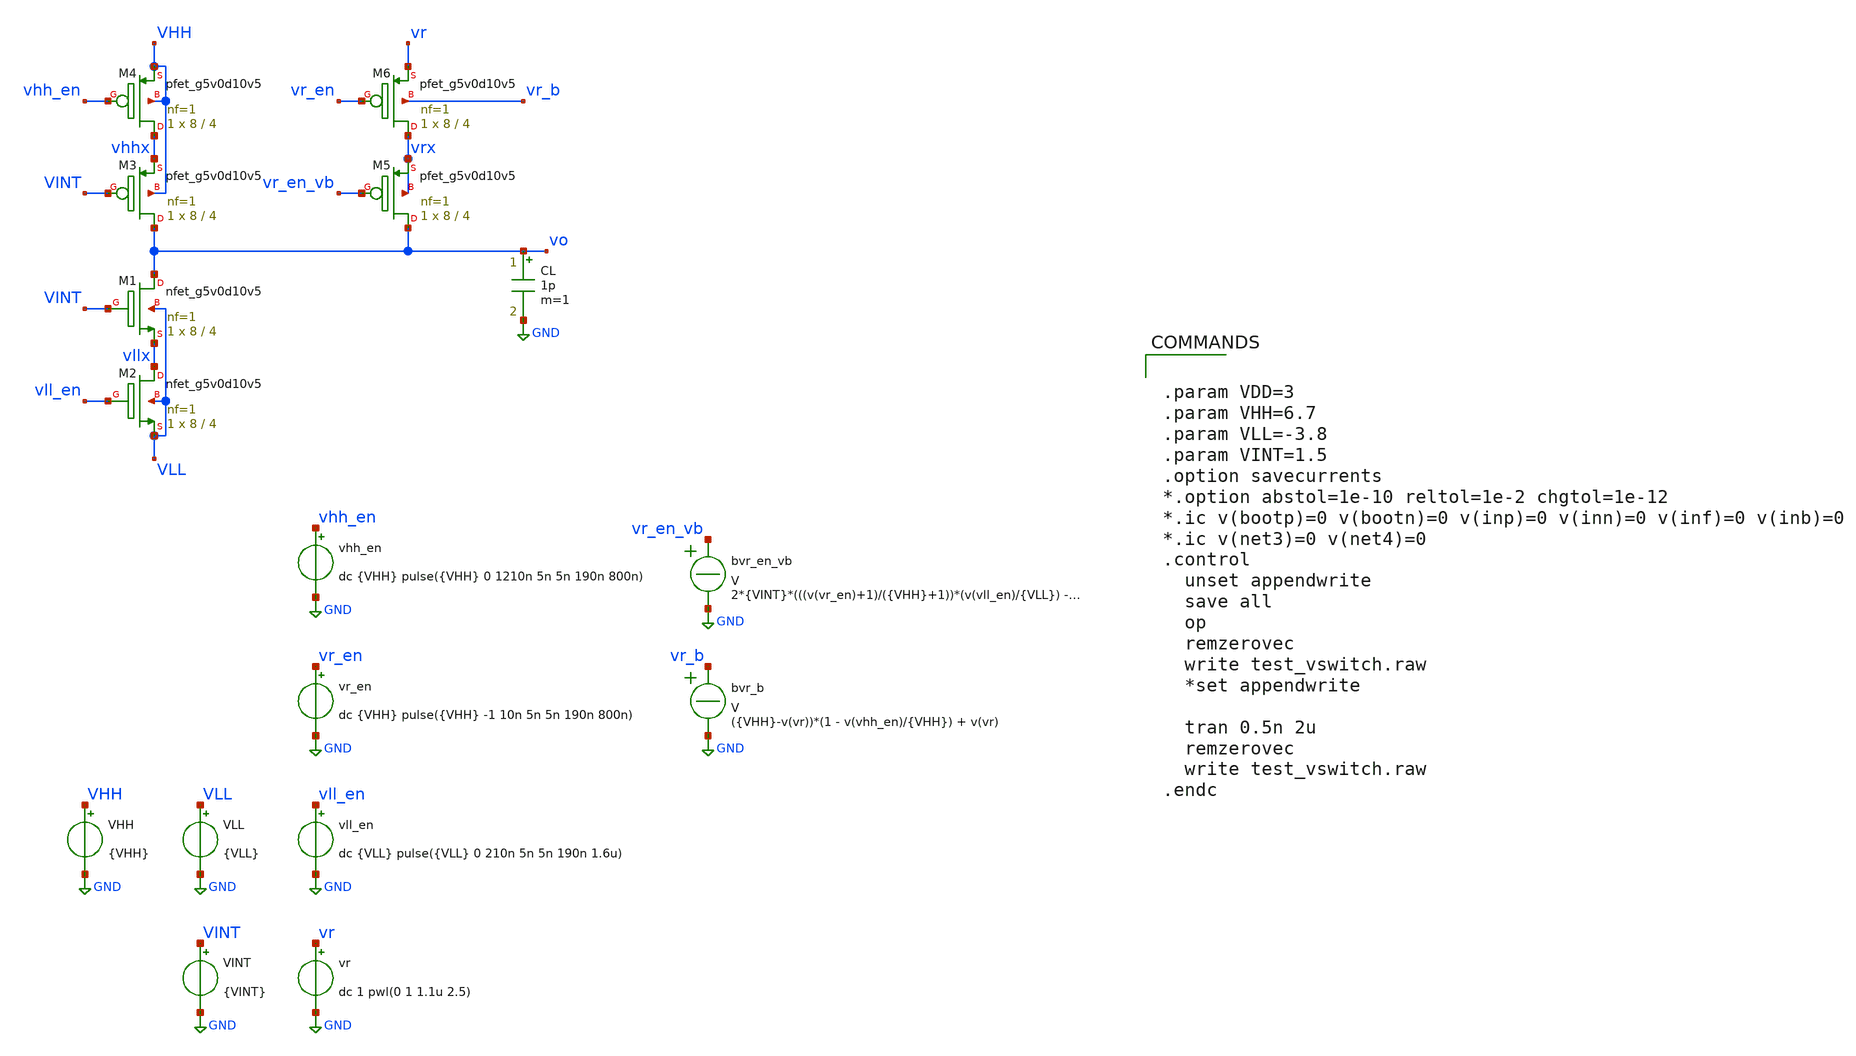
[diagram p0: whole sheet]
** sch_path: analog_switch/test_vswitch.sch
**.subckt test_vswitch
XM1 vo VINT vllx VLL sky130_fd_pr__nfet_g5v0d10v5 L=4 W=8 nf=1 ad='int((nf+1)/2) * W/nf * 0.29' as='int((nf+2)/2) * W/nf * 0.29'
+ pd='2*int((nf+1)/2) * (W/nf + 0.29)' ps='2*int((nf+2)/2) * (W/nf + 0.29)' nrd='0.29 / W' nrs='0.29 / W'
+ sa=0 sb=0 sd=0 mult=1 m=1
XM2 vllx vll_en VLL VLL sky130_fd_pr__nfet_g5v0d10v5 L=4 W=8 nf=1 ad='int((nf+1)/2) * W/nf * 0.29' as='int((nf+2)/2) * W/nf * 0.29'
+ pd='2*int((nf+1)/2) * (W/nf + 0.29)' ps='2*int((nf+2)/2) * (W/nf + 0.29)' nrd='0.29 / W' nrs='0.29 / W'
+ sa=0 sb=0 sd=0 mult=1 m=1
XM3 vo VINT vhhx VHH sky130_fd_pr__pfet_g5v0d10v5 L=4 W=8 nf=1 ad='int((nf+1)/2) * W/nf * 0.29' as='int((nf+2)/2) * W/nf * 0.29'
+ pd='2*int((nf+1)/2) * (W/nf + 0.29)' ps='2*int((nf+2)/2) * (W/nf + 0.29)' nrd='0.29 / W' nrs='0.29 / W'
+ sa=0 sb=0 sd=0 mult=1 m=1
XM4 vhhx vhh_en VHH VHH sky130_fd_pr__pfet_g5v0d10v5 L=4 W=8 nf=1 ad='int((nf+1)/2) * W/nf * 0.29' as='int((nf+2)/2) * W/nf * 0.29'
+ pd='2*int((nf+1)/2) * (W/nf + 0.29)' ps='2*int((nf+2)/2) * (W/nf + 0.29)' nrd='0.29 / W' nrs='0.29 / W'
+ sa=0 sb=0 sd=0 mult=1 m=1
XM5 vo vr_en_vb vrx vrx sky130_fd_pr__pfet_g5v0d10v5 L=4 W=8 nf=1 ad='int((nf+1)/2) * W/nf * 0.29' as='int((nf+2)/2) * W/nf * 0.29'
+ pd='2*int((nf+1)/2) * (W/nf + 0.29)' ps='2*int((nf+2)/2) * (W/nf + 0.29)' nrd='0.29 / W' nrs='0.29 / W'
+ sa=0 sb=0 sd=0 mult=1 m=1
XM6 vrx vr_en vr vr_b sky130_fd_pr__pfet_g5v0d10v5 L=4 W=8 nf=1 ad='int((nf+1)/2) * W/nf * 0.29' as='int((nf+2)/2) * W/nf * 0.29'
+ pd='2*int((nf+1)/2) * (W/nf + 0.29)' ps='2*int((nf+2)/2) * (W/nf + 0.29)' nrd='0.29 / W' nrs='0.29 / W'
+ sa=0 sb=0 sd=0 mult=1 m=1
VHH VHH GND {VHH}
VLL VLL GND {VLL}
vr vr GND dc 1 pwl(0 1 1.1u 2.5)
VINT VINT GND {VINT}
vll_en vll_en GND dc {VLL} pulse({VLL} 0 210n 5n 5n 190n 1.6u)
vr_en vr_en GND dc {VHH} pulse({VHH} -1 10n 5n 5n 190n 800n)
vhh_en vhh_en GND dc {VHH} pulse({VHH} 0 1210n 5n 5n 190n 800n)
bvr_en_vb vr_en_vb GND V = 2*{VINT}*(((v(vr_en)+1)/({VHH}+1))*(v(vll_en)/{VLL}) - 0.5)
CL vo GND 1p m=1
bvr_b vr_b GND V = ({VHH}-v(vr))*(1 - v(vhh_en)/{VHH}) + v(vr)
**** begin user architecture code

** opencircuitdesign pdks install
.lib $::SKYWATER_MODELS/sky130.lib.spice tt




.param VDD=3
.param VHH=6.7
.param VLL=-3.8
.param VINT=1.5
.option savecurrents
*.option abstol=1e-10 reltol=1e-2 chgtol=1e-12
*.ic v(bootp)=0 v(bootn)=0 v(inp)=0 v(inn)=0 v(inf)=0 v(inb)=0
*.ic v(net3)=0 v(net4)=0
.control
  unset appendwrite
  save all
  op
  remzerovec
  write test_vswitch.raw
  *set appendwrite

  tran 0.5n 2u
  remzerovec
  write test_vswitch.raw
.endc


**** end user architecture code
**.ends
.GLOBAL GND
.end
